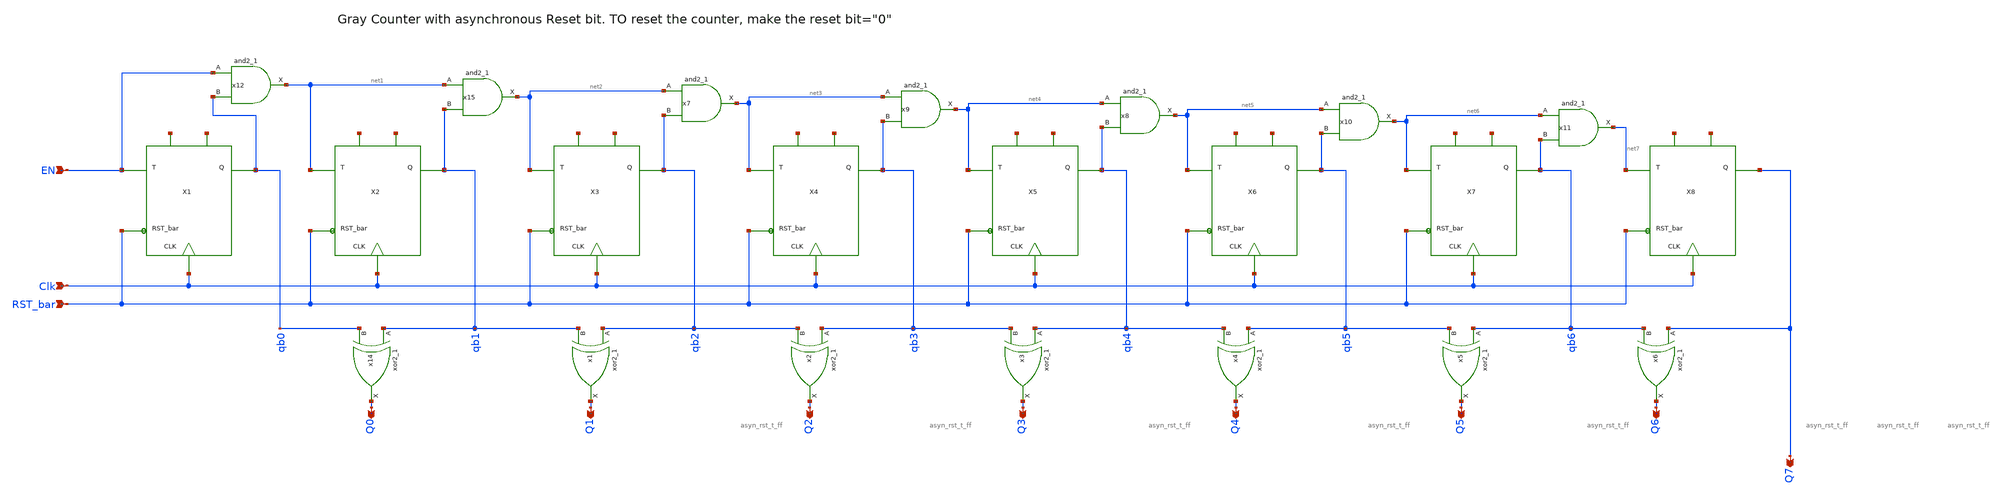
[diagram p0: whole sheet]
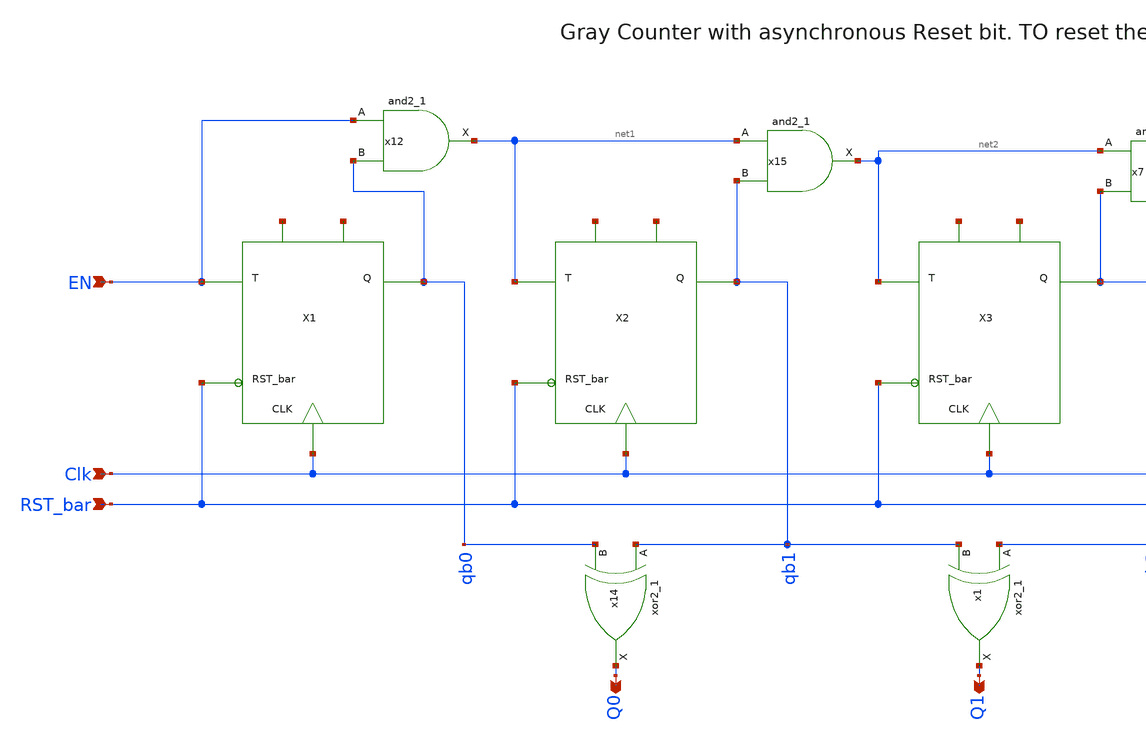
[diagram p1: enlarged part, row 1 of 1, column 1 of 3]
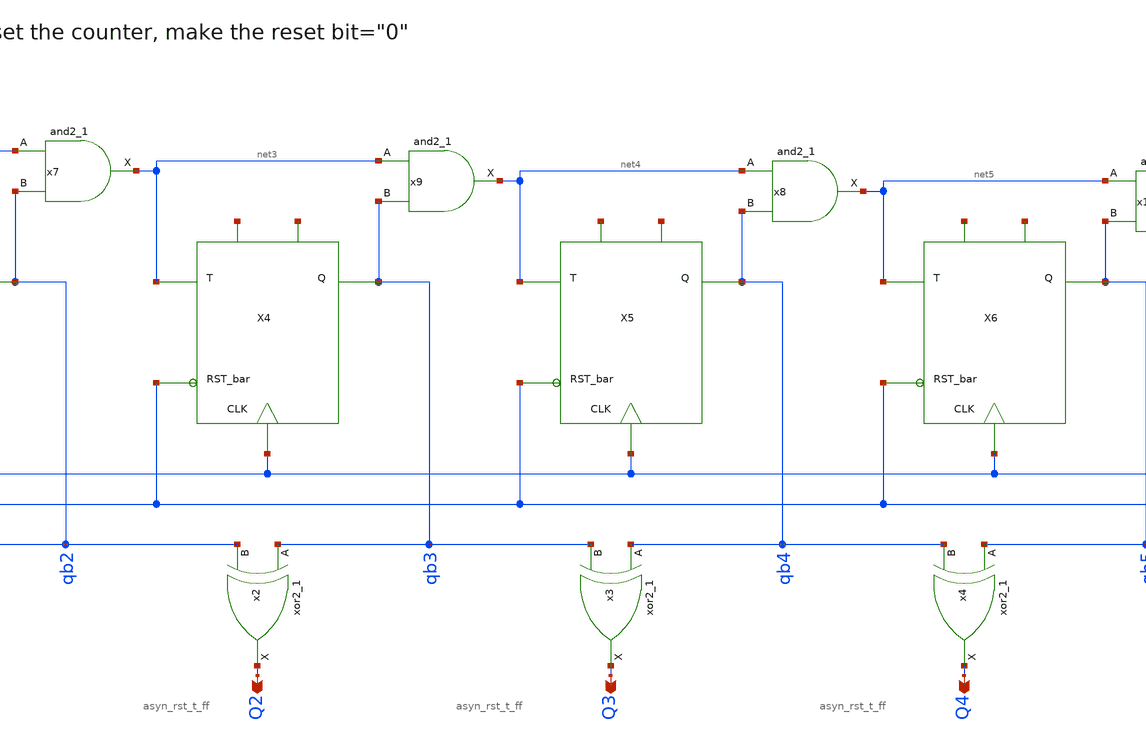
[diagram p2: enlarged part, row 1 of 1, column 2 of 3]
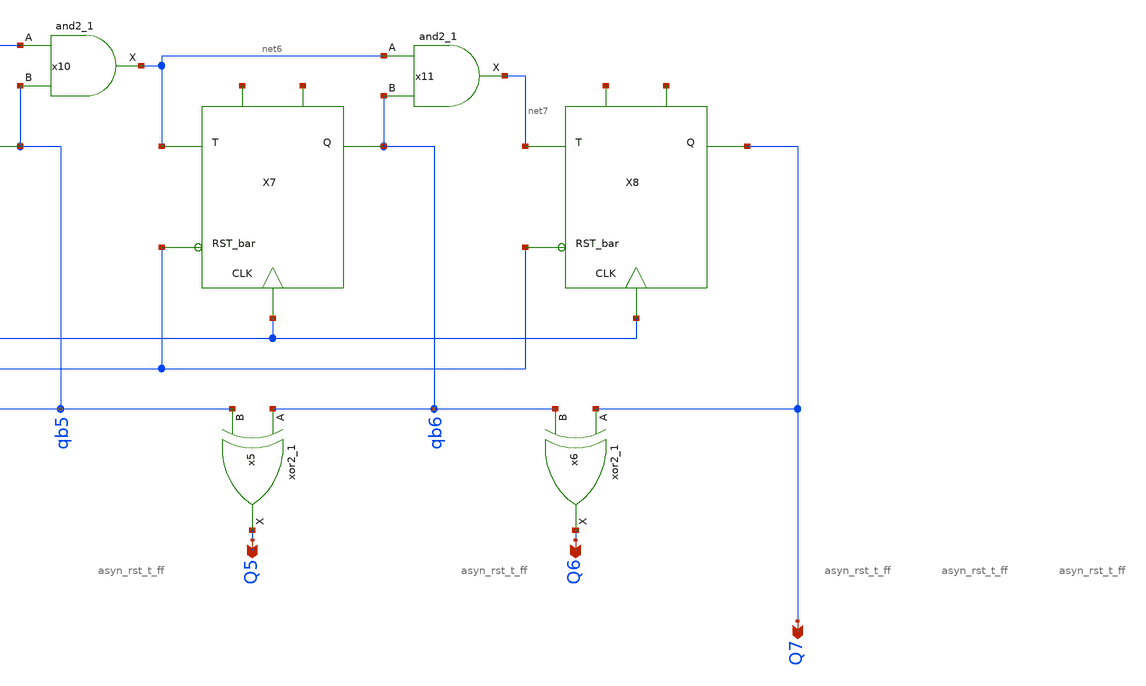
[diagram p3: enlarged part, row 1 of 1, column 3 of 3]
** sch_path: xschem/Asyn_rst_gray_counter/asyn_rst_gray_counter.sch
**.subckt asyn_rst_gray_counter Clk EN Q0 Q1 Q2 Q4 Q5 Q6 Q7 Q3 RST_bar
*.ipin Clk
*.ipin EN
*.opin Q0
*.opin Q1
*.opin Q2
*.opin Q4
*.opin Q5
*.opin Q6
*.opin Q7
*.opin Q3
*.ipin RST_bar
x14 qb1 qb0 GND GND VDD VDD Q0 sky130_fd_sc_lp__xor2_1
x15 net1 qb1 GND GND VDD VDD net2 sky130_fd_sc_lp__and2_1
x1 qb2 qb1 GND GND VDD VDD Q1 sky130_fd_sc_lp__xor2_1
x2 qb3 qb2 GND GND VDD VDD Q2 sky130_fd_sc_lp__xor2_1
x3 qb4 qb3 GND GND VDD VDD Q3 sky130_fd_sc_lp__xor2_1
x4 qb5 qb4 GND GND VDD VDD Q4 sky130_fd_sc_lp__xor2_1
x5 qb6 qb5 GND GND VDD VDD Q5 sky130_fd_sc_lp__xor2_1
x6 Q7 qb6 GND GND VDD VDD Q6 sky130_fd_sc_lp__xor2_1
x7 net2 qb2 GND GND VDD VDD net3 sky130_fd_sc_lp__and2_1
x8 net4 qb4 GND GND VDD VDD net5 sky130_fd_sc_lp__and2_1
x9 net3 qb3 GND GND VDD VDD net4 sky130_fd_sc_lp__and2_1
x10 net5 qb5 GND GND VDD VDD net6 sky130_fd_sc_lp__and2_1
x11 net6 qb6 GND GND VDD VDD net7 sky130_fd_sc_lp__and2_1
x12 EN qb0 GND GND VDD VDD net1 sky130_fd_sc_lp__and2_1
X1 EN qb0 Clk RST_bar net8 net9 asyn_rst_t_ff
X2 net1 qb1 Clk RST_bar net10 net11 asyn_rst_t_ff
X3 net2 qb2 Clk RST_bar net12 net13 asyn_rst_t_ff
X4 net3 qb3 Clk RST_bar net14 net15 asyn_rst_t_ff
X5 net4 qb4 Clk RST_bar net16 net17 asyn_rst_t_ff
X6 net5 qb5 Clk RST_bar net18 net19 asyn_rst_t_ff
X7 net6 qb6 Clk RST_bar net20 net21 asyn_rst_t_ff
X8 net7 Q7 Clk RST_bar net22 net23 asyn_rst_t_ff
**.ends

* expanding   symbol:  T_flip_flop/asyn_rst_t_ff.sym # of pins=6
** sym_path: xschem/T_flip_flop/asyn_rst_t_ff.sym
** sch_path: xschem/T_flip_flop/asyn_rst_t_ff.sch
.subckt asyn_rst_t_ff T Q CLK RST_bar GND VDD
*.ipin T
*.ipin CLK
*.opin Q
*.ipin RST_bar
*.iopin VDD
*.iopin GND
x1 CLK net1 RST_bar GND GND VDD VDD Q sky130_fd_sc_lp__dfrtp_1
x3 T Q GND GND VDD VDD net1 sky130_fd_sc_lp__xor2_1
.ends

.end
